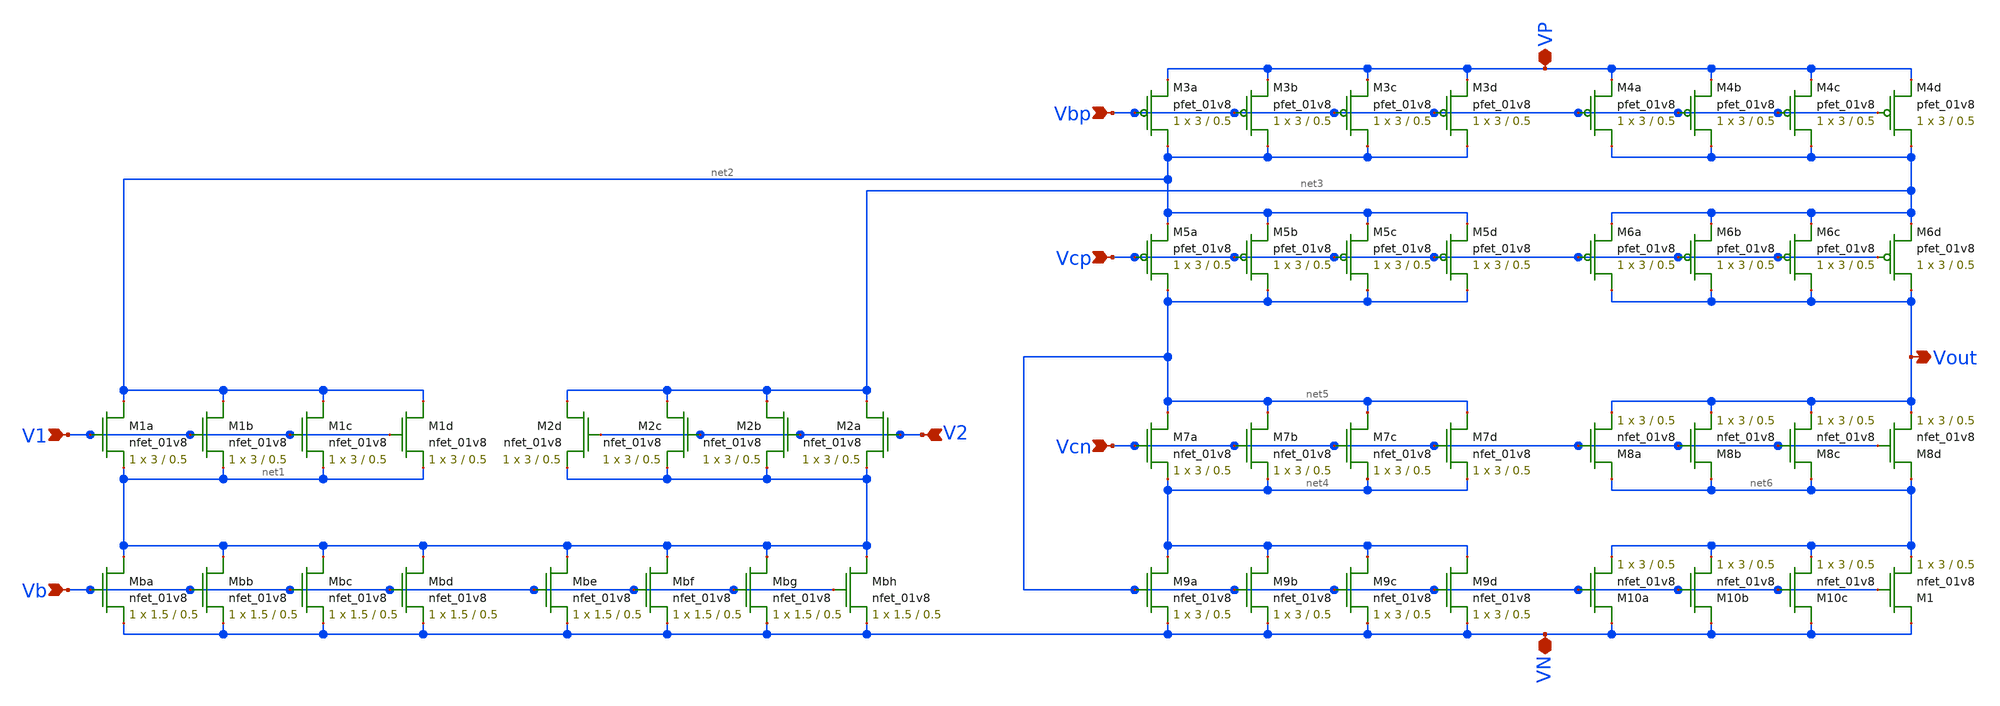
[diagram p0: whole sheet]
** sch_path: mp3/xschem/opamp_schematic.sch
**.subckt opamp_schematic Vbp Vcp Vcn V2 V1 Vb VP VN Vout
*.ipin Vbp
*.ipin Vcp
*.ipin Vcn
*.ipin V2
*.ipin V1
*.ipin Vb
*.iopin VP
*.iopin VN
*.opin Vout
XM1a net2 V1 net1 GND sky130_fd_pr__nfet_01v8 L=0.5 W=3 nf=1 ad='int((nf+1)/2) * W/nf * 0.29' as='int((nf+2)/2) * W/nf * 0.29'
+ pd='2*int((nf+1)/2) * (W/nf + 0.29)' ps='2*int((nf+2)/2) * (W/nf + 0.29)' nrd='0.29 / W' nrs='0.29 / W'
+ sa=0 sb=0 sd=0 mult=1 m=1
XM1b net2 V1 net1 GND sky130_fd_pr__nfet_01v8 L=0.5 W=3 nf=1 ad='int((nf+1)/2) * W/nf * 0.29' as='int((nf+2)/2) * W/nf * 0.29'
+ pd='2*int((nf+1)/2) * (W/nf + 0.29)' ps='2*int((nf+2)/2) * (W/nf + 0.29)' nrd='0.29 / W' nrs='0.29 / W'
+ sa=0 sb=0 sd=0 mult=1 m=1
XM1c net2 V1 net1 GND sky130_fd_pr__nfet_01v8 L=0.5 W=3 nf=1 ad='int((nf+1)/2) * W/nf * 0.29' as='int((nf+2)/2) * W/nf * 0.29'
+ pd='2*int((nf+1)/2) * (W/nf + 0.29)' ps='2*int((nf+2)/2) * (W/nf + 0.29)' nrd='0.29 / W' nrs='0.29 / W'
+ sa=0 sb=0 sd=0 mult=1 m=1
XM1d net2 V1 net1 GND sky130_fd_pr__nfet_01v8 L=0.5 W=3 nf=1 ad='int((nf+1)/2) * W/nf * 0.29' as='int((nf+2)/2) * W/nf * 0.29'
+ pd='2*int((nf+1)/2) * (W/nf + 0.29)' ps='2*int((nf+2)/2) * (W/nf + 0.29)' nrd='0.29 / W' nrs='0.29 / W'
+ sa=0 sb=0 sd=0 mult=1 m=1
XM2a net3 V2 net1 GND sky130_fd_pr__nfet_01v8 L=0.5 W=3 nf=1 ad='int((nf+1)/2) * W/nf * 0.29' as='int((nf+2)/2) * W/nf * 0.29'
+ pd='2*int((nf+1)/2) * (W/nf + 0.29)' ps='2*int((nf+2)/2) * (W/nf + 0.29)' nrd='0.29 / W' nrs='0.29 / W'
+ sa=0 sb=0 sd=0 mult=1 m=1
XM2b net3 V2 net1 GND sky130_fd_pr__nfet_01v8 L=0.5 W=3 nf=1 ad='int((nf+1)/2) * W/nf * 0.29' as='int((nf+2)/2) * W/nf * 0.29'
+ pd='2*int((nf+1)/2) * (W/nf + 0.29)' ps='2*int((nf+2)/2) * (W/nf + 0.29)' nrd='0.29 / W' nrs='0.29 / W'
+ sa=0 sb=0 sd=0 mult=1 m=1
XM2c net3 V2 net1 GND sky130_fd_pr__nfet_01v8 L=0.5 W=3 nf=1 ad='int((nf+1)/2) * W/nf * 0.29' as='int((nf+2)/2) * W/nf * 0.29'
+ pd='2*int((nf+1)/2) * (W/nf + 0.29)' ps='2*int((nf+2)/2) * (W/nf + 0.29)' nrd='0.29 / W' nrs='0.29 / W'
+ sa=0 sb=0 sd=0 mult=1 m=1
XM2d net3 V2 net1 GND sky130_fd_pr__nfet_01v8 L=0.5 W=3 nf=1 ad='int((nf+1)/2) * W/nf * 0.29' as='int((nf+2)/2) * W/nf * 0.29'
+ pd='2*int((nf+1)/2) * (W/nf + 0.29)' ps='2*int((nf+2)/2) * (W/nf + 0.29)' nrd='0.29 / W' nrs='0.29 / W'
+ sa=0 sb=0 sd=0 mult=1 m=1
XMba net1 Vb VN GND sky130_fd_pr__nfet_01v8 L=0.5 W=1.5 nf=1 ad='int((nf+1)/2) * W/nf * 0.29' as='int((nf+2)/2) * W/nf * 0.29'
+ pd='2*int((nf+1)/2) * (W/nf + 0.29)' ps='2*int((nf+2)/2) * (W/nf + 0.29)' nrd='0.29 / W' nrs='0.29 / W'
+ sa=0 sb=0 sd=0 mult=1 m=1
XMbb net1 Vb VN GND sky130_fd_pr__nfet_01v8 L=0.5 W=1.5 nf=1 ad='int((nf+1)/2) * W/nf * 0.29' as='int((nf+2)/2) * W/nf * 0.29'
+ pd='2*int((nf+1)/2) * (W/nf + 0.29)' ps='2*int((nf+2)/2) * (W/nf + 0.29)' nrd='0.29 / W' nrs='0.29 / W'
+ sa=0 sb=0 sd=0 mult=1 m=1
XMbc net1 Vb VN GND sky130_fd_pr__nfet_01v8 L=0.5 W=1.5 nf=1 ad='int((nf+1)/2) * W/nf * 0.29' as='int((nf+2)/2) * W/nf * 0.29'
+ pd='2*int((nf+1)/2) * (W/nf + 0.29)' ps='2*int((nf+2)/2) * (W/nf + 0.29)' nrd='0.29 / W' nrs='0.29 / W'
+ sa=0 sb=0 sd=0 mult=1 m=1
XMbd net1 Vb VN GND sky130_fd_pr__nfet_01v8 L=0.5 W=1.5 nf=1 ad='int((nf+1)/2) * W/nf * 0.29' as='int((nf+2)/2) * W/nf * 0.29'
+ pd='2*int((nf+1)/2) * (W/nf + 0.29)' ps='2*int((nf+2)/2) * (W/nf + 0.29)' nrd='0.29 / W' nrs='0.29 / W'
+ sa=0 sb=0 sd=0 mult=1 m=1
XMbe net1 Vb VN GND sky130_fd_pr__nfet_01v8 L=0.5 W=1.5 nf=1 ad='int((nf+1)/2) * W/nf * 0.29' as='int((nf+2)/2) * W/nf * 0.29'
+ pd='2*int((nf+1)/2) * (W/nf + 0.29)' ps='2*int((nf+2)/2) * (W/nf + 0.29)' nrd='0.29 / W' nrs='0.29 / W'
+ sa=0 sb=0 sd=0 mult=1 m=1
XMbf net1 Vb VN GND sky130_fd_pr__nfet_01v8 L=0.5 W=1.5 nf=1 ad='int((nf+1)/2) * W/nf * 0.29' as='int((nf+2)/2) * W/nf * 0.29'
+ pd='2*int((nf+1)/2) * (W/nf + 0.29)' ps='2*int((nf+2)/2) * (W/nf + 0.29)' nrd='0.29 / W' nrs='0.29 / W'
+ sa=0 sb=0 sd=0 mult=1 m=1
XMbg net1 Vb VN GND sky130_fd_pr__nfet_01v8 L=0.5 W=1.5 nf=1 ad='int((nf+1)/2) * W/nf * 0.29' as='int((nf+2)/2) * W/nf * 0.29'
+ pd='2*int((nf+1)/2) * (W/nf + 0.29)' ps='2*int((nf+2)/2) * (W/nf + 0.29)' nrd='0.29 / W' nrs='0.29 / W'
+ sa=0 sb=0 sd=0 mult=1 m=1
XMbh net1 Vb VN GND sky130_fd_pr__nfet_01v8 L=0.5 W=1.5 nf=1 ad='int((nf+1)/2) * W/nf * 0.29' as='int((nf+2)/2) * W/nf * 0.29'
+ pd='2*int((nf+1)/2) * (W/nf + 0.29)' ps='2*int((nf+2)/2) * (W/nf + 0.29)' nrd='0.29 / W' nrs='0.29 / W'
+ sa=0 sb=0 sd=0 mult=1 m=1
XM7a net5 Vcn net4 GND sky130_fd_pr__nfet_01v8 L=0.5 W=3 nf=1 ad='int((nf+1)/2) * W/nf * 0.29' as='int((nf+2)/2) * W/nf * 0.29'
+ pd='2*int((nf+1)/2) * (W/nf + 0.29)' ps='2*int((nf+2)/2) * (W/nf + 0.29)' nrd='0.29 / W' nrs='0.29 / W'
+ sa=0 sb=0 sd=0 mult=1 m=1
XM7b net5 Vcn net4 GND sky130_fd_pr__nfet_01v8 L=0.5 W=3 nf=1 ad='int((nf+1)/2) * W/nf * 0.29' as='int((nf+2)/2) * W/nf * 0.29'
+ pd='2*int((nf+1)/2) * (W/nf + 0.29)' ps='2*int((nf+2)/2) * (W/nf + 0.29)' nrd='0.29 / W' nrs='0.29 / W'
+ sa=0 sb=0 sd=0 mult=1 m=1
XM7c net5 Vcn net4 GND sky130_fd_pr__nfet_01v8 L=0.5 W=3 nf=1 ad='int((nf+1)/2) * W/nf * 0.29' as='int((nf+2)/2) * W/nf * 0.29'
+ pd='2*int((nf+1)/2) * (W/nf + 0.29)' ps='2*int((nf+2)/2) * (W/nf + 0.29)' nrd='0.29 / W' nrs='0.29 / W'
+ sa=0 sb=0 sd=0 mult=1 m=1
XM7d net5 Vcn net4 GND sky130_fd_pr__nfet_01v8 L=0.5 W=3 nf=1 ad='int((nf+1)/2) * W/nf * 0.29' as='int((nf+2)/2) * W/nf * 0.29'
+ pd='2*int((nf+1)/2) * (W/nf + 0.29)' ps='2*int((nf+2)/2) * (W/nf + 0.29)' nrd='0.29 / W' nrs='0.29 / W'
+ sa=0 sb=0 sd=0 mult=1 m=1
XM8a net6 Vcn Vout GND sky130_fd_pr__nfet_01v8 L=0.5 W=3 nf=1 ad='int((nf+1)/2) * W/nf * 0.29' as='int((nf+2)/2) * W/nf * 0.29'
+ pd='2*int((nf+1)/2) * (W/nf + 0.29)' ps='2*int((nf+2)/2) * (W/nf + 0.29)' nrd='0.29 / W' nrs='0.29 / W'
+ sa=0 sb=0 sd=0 mult=1 m=1
XM8b net6 Vcn Vout GND sky130_fd_pr__nfet_01v8 L=0.5 W=3 nf=1 ad='int((nf+1)/2) * W/nf * 0.29' as='int((nf+2)/2) * W/nf * 0.29'
+ pd='2*int((nf+1)/2) * (W/nf + 0.29)' ps='2*int((nf+2)/2) * (W/nf + 0.29)' nrd='0.29 / W' nrs='0.29 / W'
+ sa=0 sb=0 sd=0 mult=1 m=1
XM8c net6 Vcn Vout GND sky130_fd_pr__nfet_01v8 L=0.5 W=3 nf=1 ad='int((nf+1)/2) * W/nf * 0.29' as='int((nf+2)/2) * W/nf * 0.29'
+ pd='2*int((nf+1)/2) * (W/nf + 0.29)' ps='2*int((nf+2)/2) * (W/nf + 0.29)' nrd='0.29 / W' nrs='0.29 / W'
+ sa=0 sb=0 sd=0 mult=1 m=1
XM8d net6 Vcn Vout GND sky130_fd_pr__nfet_01v8 L=0.5 W=3 nf=1 ad='int((nf+1)/2) * W/nf * 0.29' as='int((nf+2)/2) * W/nf * 0.29'
+ pd='2*int((nf+1)/2) * (W/nf + 0.29)' ps='2*int((nf+2)/2) * (W/nf + 0.29)' nrd='0.29 / W' nrs='0.29 / W'
+ sa=0 sb=0 sd=0 mult=1 m=1
XM9a net4 net5 VN GND sky130_fd_pr__nfet_01v8 L=0.5 W=3 nf=1 ad='int((nf+1)/2) * W/nf * 0.29' as='int((nf+2)/2) * W/nf * 0.29'
+ pd='2*int((nf+1)/2) * (W/nf + 0.29)' ps='2*int((nf+2)/2) * (W/nf + 0.29)' nrd='0.29 / W' nrs='0.29 / W'
+ sa=0 sb=0 sd=0 mult=1 m=1
XM9b net4 net5 VN GND sky130_fd_pr__nfet_01v8 L=0.5 W=3 nf=1 ad='int((nf+1)/2) * W/nf * 0.29' as='int((nf+2)/2) * W/nf * 0.29'
+ pd='2*int((nf+1)/2) * (W/nf + 0.29)' ps='2*int((nf+2)/2) * (W/nf + 0.29)' nrd='0.29 / W' nrs='0.29 / W'
+ sa=0 sb=0 sd=0 mult=1 m=1
XM9c net4 net5 VN GND sky130_fd_pr__nfet_01v8 L=0.5 W=3 nf=1 ad='int((nf+1)/2) * W/nf * 0.29' as='int((nf+2)/2) * W/nf * 0.29'
+ pd='2*int((nf+1)/2) * (W/nf + 0.29)' ps='2*int((nf+2)/2) * (W/nf + 0.29)' nrd='0.29 / W' nrs='0.29 / W'
+ sa=0 sb=0 sd=0 mult=1 m=1
XM9d net4 net5 VN GND sky130_fd_pr__nfet_01v8 L=0.5 W=3 nf=1 ad='int((nf+1)/2) * W/nf * 0.29' as='int((nf+2)/2) * W/nf * 0.29'
+ pd='2*int((nf+1)/2) * (W/nf + 0.29)' ps='2*int((nf+2)/2) * (W/nf + 0.29)' nrd='0.29 / W' nrs='0.29 / W'
+ sa=0 sb=0 sd=0 mult=1 m=1
XM10a VN net5 net6 GND sky130_fd_pr__nfet_01v8 L=0.5 W=3 nf=1 ad='int((nf+1)/2) * W/nf * 0.29' as='int((nf+2)/2) * W/nf * 0.29'
+ pd='2*int((nf+1)/2) * (W/nf + 0.29)' ps='2*int((nf+2)/2) * (W/nf + 0.29)' nrd='0.29 / W' nrs='0.29 / W'
+ sa=0 sb=0 sd=0 mult=1 m=1
XM10b VN net5 net6 GND sky130_fd_pr__nfet_01v8 L=0.5 W=3 nf=1 ad='int((nf+1)/2) * W/nf * 0.29' as='int((nf+2)/2) * W/nf * 0.29'
+ pd='2*int((nf+1)/2) * (W/nf + 0.29)' ps='2*int((nf+2)/2) * (W/nf + 0.29)' nrd='0.29 / W' nrs='0.29 / W'
+ sa=0 sb=0 sd=0 mult=1 m=1
XM10c VN net5 net6 GND sky130_fd_pr__nfet_01v8 L=0.5 W=3 nf=1 ad='int((nf+1)/2) * W/nf * 0.29' as='int((nf+2)/2) * W/nf * 0.29'
+ pd='2*int((nf+1)/2) * (W/nf + 0.29)' ps='2*int((nf+2)/2) * (W/nf + 0.29)' nrd='0.29 / W' nrs='0.29 / W'
+ sa=0 sb=0 sd=0 mult=1 m=1
XM1 VN net5 net6 GND sky130_fd_pr__nfet_01v8 L=0.5 W=3 nf=1 ad='int((nf+1)/2) * W/nf * 0.29' as='int((nf+2)/2) * W/nf * 0.29'
+ pd='2*int((nf+1)/2) * (W/nf + 0.29)' ps='2*int((nf+2)/2) * (W/nf + 0.29)' nrd='0.29 / W' nrs='0.29 / W'
+ sa=0 sb=0 sd=0 mult=1 m=1
XM5a net5 Vcp net2 VDD sky130_fd_pr__pfet_01v8 L=0.5 W=3 nf=1 ad='int((nf+1)/2) * W/nf * 0.29' as='int((nf+2)/2) * W/nf * 0.29'
+ pd='2*int((nf+1)/2) * (W/nf + 0.29)' ps='2*int((nf+2)/2) * (W/nf + 0.29)' nrd='0.29 / W' nrs='0.29 / W'
+ sa=0 sb=0 sd=0 mult=1 m=1
XM5b net5 Vcp net2 VDD sky130_fd_pr__pfet_01v8 L=0.5 W=3 nf=1 ad='int((nf+1)/2) * W/nf * 0.29' as='int((nf+2)/2) * W/nf * 0.29'
+ pd='2*int((nf+1)/2) * (W/nf + 0.29)' ps='2*int((nf+2)/2) * (W/nf + 0.29)' nrd='0.29 / W' nrs='0.29 / W'
+ sa=0 sb=0 sd=0 mult=1 m=1
XM5c net5 Vcp net2 VDD sky130_fd_pr__pfet_01v8 L=0.5 W=3 nf=1 ad='int((nf+1)/2) * W/nf * 0.29' as='int((nf+2)/2) * W/nf * 0.29'
+ pd='2*int((nf+1)/2) * (W/nf + 0.29)' ps='2*int((nf+2)/2) * (W/nf + 0.29)' nrd='0.29 / W' nrs='0.29 / W'
+ sa=0 sb=0 sd=0 mult=1 m=1
XM5d net5 Vcp net2 VDD sky130_fd_pr__pfet_01v8 L=0.5 W=3 nf=1 ad='int((nf+1)/2) * W/nf * 0.29' as='int((nf+2)/2) * W/nf * 0.29'
+ pd='2*int((nf+1)/2) * (W/nf + 0.29)' ps='2*int((nf+2)/2) * (W/nf + 0.29)' nrd='0.29 / W' nrs='0.29 / W'
+ sa=0 sb=0 sd=0 mult=1 m=1
XM6a Vout Vcp net3 VDD sky130_fd_pr__pfet_01v8 L=0.5 W=3 nf=1 ad='int((nf+1)/2) * W/nf * 0.29' as='int((nf+2)/2) * W/nf * 0.29'
+ pd='2*int((nf+1)/2) * (W/nf + 0.29)' ps='2*int((nf+2)/2) * (W/nf + 0.29)' nrd='0.29 / W' nrs='0.29 / W'
+ sa=0 sb=0 sd=0 mult=1 m=1
XM6b Vout Vcp net3 VDD sky130_fd_pr__pfet_01v8 L=0.5 W=3 nf=1 ad='int((nf+1)/2) * W/nf * 0.29' as='int((nf+2)/2) * W/nf * 0.29'
+ pd='2*int((nf+1)/2) * (W/nf + 0.29)' ps='2*int((nf+2)/2) * (W/nf + 0.29)' nrd='0.29 / W' nrs='0.29 / W'
+ sa=0 sb=0 sd=0 mult=1 m=1
XM6c Vout Vcp net3 VDD sky130_fd_pr__pfet_01v8 L=0.5 W=3 nf=1 ad='int((nf+1)/2) * W/nf * 0.29' as='int((nf+2)/2) * W/nf * 0.29'
+ pd='2*int((nf+1)/2) * (W/nf + 0.29)' ps='2*int((nf+2)/2) * (W/nf + 0.29)' nrd='0.29 / W' nrs='0.29 / W'
+ sa=0 sb=0 sd=0 mult=1 m=1
XM6d Vout Vcp net3 VDD sky130_fd_pr__pfet_01v8 L=0.5 W=3 nf=1 ad='int((nf+1)/2) * W/nf * 0.29' as='int((nf+2)/2) * W/nf * 0.29'
+ pd='2*int((nf+1)/2) * (W/nf + 0.29)' ps='2*int((nf+2)/2) * (W/nf + 0.29)' nrd='0.29 / W' nrs='0.29 / W'
+ sa=0 sb=0 sd=0 mult=1 m=1
XM3a net2 Vbp VP VDD sky130_fd_pr__pfet_01v8 L=0.5 W=3 nf=1 ad='int((nf+1)/2) * W/nf * 0.29' as='int((nf+2)/2) * W/nf * 0.29'
+ pd='2*int((nf+1)/2) * (W/nf + 0.29)' ps='2*int((nf+2)/2) * (W/nf + 0.29)' nrd='0.29 / W' nrs='0.29 / W'
+ sa=0 sb=0 sd=0 mult=1 m=1
XM3b net2 Vbp VP VDD sky130_fd_pr__pfet_01v8 L=0.5 W=3 nf=1 ad='int((nf+1)/2) * W/nf * 0.29' as='int((nf+2)/2) * W/nf * 0.29'
+ pd='2*int((nf+1)/2) * (W/nf + 0.29)' ps='2*int((nf+2)/2) * (W/nf + 0.29)' nrd='0.29 / W' nrs='0.29 / W'
+ sa=0 sb=0 sd=0 mult=1 m=1
XM3c net2 Vbp VP VDD sky130_fd_pr__pfet_01v8 L=0.5 W=3 nf=1 ad='int((nf+1)/2) * W/nf * 0.29' as='int((nf+2)/2) * W/nf * 0.29'
+ pd='2*int((nf+1)/2) * (W/nf + 0.29)' ps='2*int((nf+2)/2) * (W/nf + 0.29)' nrd='0.29 / W' nrs='0.29 / W'
+ sa=0 sb=0 sd=0 mult=1 m=1
XM3d net2 Vbp VP VDD sky130_fd_pr__pfet_01v8 L=0.5 W=3 nf=1 ad='int((nf+1)/2) * W/nf * 0.29' as='int((nf+2)/2) * W/nf * 0.29'
+ pd='2*int((nf+1)/2) * (W/nf + 0.29)' ps='2*int((nf+2)/2) * (W/nf + 0.29)' nrd='0.29 / W' nrs='0.29 / W'
+ sa=0 sb=0 sd=0 mult=1 m=1
XM4a net3 Vbp VP VDD sky130_fd_pr__pfet_01v8 L=0.5 W=3 nf=1 ad='int((nf+1)/2) * W/nf * 0.29' as='int((nf+2)/2) * W/nf * 0.29'
+ pd='2*int((nf+1)/2) * (W/nf + 0.29)' ps='2*int((nf+2)/2) * (W/nf + 0.29)' nrd='0.29 / W' nrs='0.29 / W'
+ sa=0 sb=0 sd=0 mult=1 m=1
XM4b net3 Vbp VP VDD sky130_fd_pr__pfet_01v8 L=0.5 W=3 nf=1 ad='int((nf+1)/2) * W/nf * 0.29' as='int((nf+2)/2) * W/nf * 0.29'
+ pd='2*int((nf+1)/2) * (W/nf + 0.29)' ps='2*int((nf+2)/2) * (W/nf + 0.29)' nrd='0.29 / W' nrs='0.29 / W'
+ sa=0 sb=0 sd=0 mult=1 m=1
XM4c net3 Vbp VP VDD sky130_fd_pr__pfet_01v8 L=0.5 W=3 nf=1 ad='int((nf+1)/2) * W/nf * 0.29' as='int((nf+2)/2) * W/nf * 0.29'
+ pd='2*int((nf+1)/2) * (W/nf + 0.29)' ps='2*int((nf+2)/2) * (W/nf + 0.29)' nrd='0.29 / W' nrs='0.29 / W'
+ sa=0 sb=0 sd=0 mult=1 m=1
XM4d net3 Vbp VP VDD sky130_fd_pr__pfet_01v8 L=0.5 W=3 nf=1 ad='int((nf+1)/2) * W/nf * 0.29' as='int((nf+2)/2) * W/nf * 0.29'
+ pd='2*int((nf+1)/2) * (W/nf + 0.29)' ps='2*int((nf+2)/2) * (W/nf + 0.29)' nrd='0.29 / W' nrs='0.29 / W'
+ sa=0 sb=0 sd=0 mult=1 m=1
**.ends
.end
